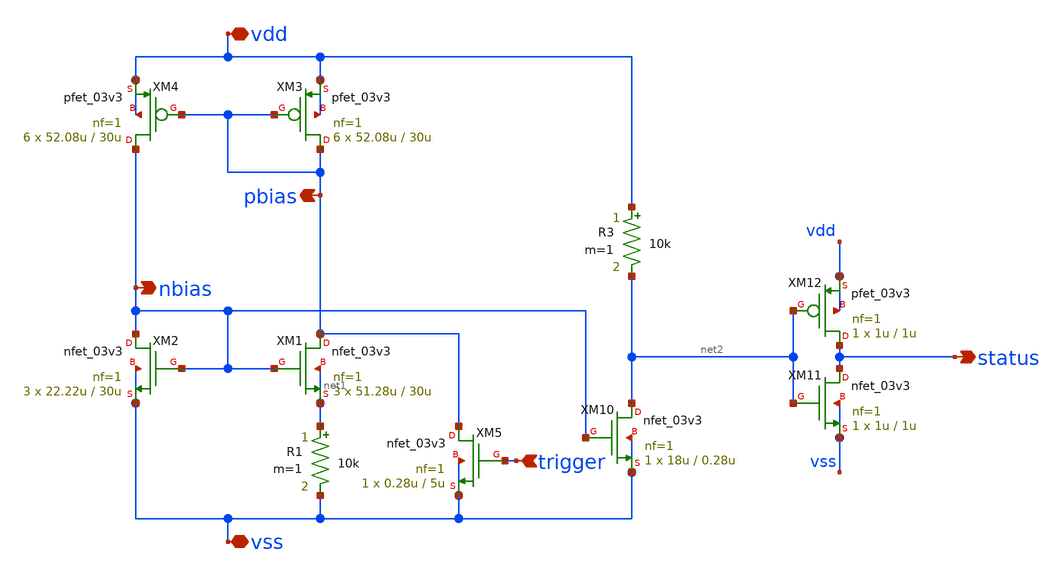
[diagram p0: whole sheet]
** sch_path: design/analog/beta multiplier/beta_multiplier.sch
**.subckt beta_multiplier vdd vss pbias nbias status trigger
*.iopin vdd
*.iopin vss
*.opin pbias
*.opin nbias
*.opin status
*.ipin trigger
XM1 pbias nbias net1 net1 nfet_03v3 L=30u W=51.28u nf=1 ad='int((nf+1)/2) * W/nf * 0.18u' as='int((nf+2)/2) * W/nf * 0.18u'
+ pd='2*int((nf+1)/2) * (W/nf + 0.18u)' ps='2*int((nf+2)/2) * (W/nf + 0.18u)' nrd='0.18u / W' nrs='0.18u / W'
+ sa=0 sb=0 sd=0 m=3
XM2 nbias nbias vss vss nfet_03v3 L=30u W=22.22u nf=1 ad='int((nf+1)/2) * W/nf * 0.18u' as='int((nf+2)/2) * W/nf * 0.18u'
+ pd='2*int((nf+1)/2) * (W/nf + 0.18u)' ps='2*int((nf+2)/2) * (W/nf + 0.18u)' nrd='0.18u / W' nrs='0.18u / W'
+ sa=0 sb=0 sd=0 m=3
XM3 pbias pbias vdd vdd pfet_03v3 L=30u W=52.08u nf=1 ad='int((nf+1)/2) * W/nf * 0.18u' as='int((nf+2)/2) * W/nf * 0.18u'
+ pd='2*int((nf+1)/2) * (W/nf + 0.18u)' ps='2*int((nf+2)/2) * (W/nf + 0.18u)' nrd='0.18u / W' nrs='0.18u / W'
+ sa=0 sb=0 sd=0 m=6
XM4 nbias pbias vdd vdd pfet_03v3 L=30u W=52.08u nf=1 ad='int((nf+1)/2) * W/nf * 0.18u' as='int((nf+2)/2) * W/nf * 0.18u'
+ pd='2*int((nf+1)/2) * (W/nf + 0.18u)' ps='2*int((nf+2)/2) * (W/nf + 0.18u)' nrd='0.18u / W' nrs='0.18u / W'
+ sa=0 sb=0 sd=0 m=6
R1 net1 vss 10k m=1
XM5 pbias trigger vss vss nfet_03v3 L=5u W=0.28u nf=1 ad='int((nf+1)/2) * W/nf * 0.18u' as='int((nf+2)/2) * W/nf * 0.18u'
+ pd='2*int((nf+1)/2) * (W/nf + 0.18u)' ps='2*int((nf+2)/2) * (W/nf + 0.18u)' nrd='0.18u / W' nrs='0.18u / W'
+ sa=0 sb=0 sd=0 m=1
XM10 net2 nbias vss vss nfet_03v3 L=0.28u W=18u nf=1 ad='int((nf+1)/2) * W/nf * 0.18u' as='int((nf+2)/2) * W/nf * 0.18u'
+ pd='2*int((nf+1)/2) * (W/nf + 0.18u)' ps='2*int((nf+2)/2) * (W/nf + 0.18u)' nrd='0.18u / W' nrs='0.18u / W'
+ sa=0 sb=0 sd=0 m=1
R3 vdd net2 10k m=1
XM11 status net2 vss vss nfet_03v3 L=1u W=1u nf=1 ad='int((nf+1)/2) * W/nf * 0.18u' as='int((nf+2)/2) * W/nf * 0.18u'
+ pd='2*int((nf+1)/2) * (W/nf + 0.18u)' ps='2*int((nf+2)/2) * (W/nf + 0.18u)' nrd='0.18u / W' nrs='0.18u / W'
+ sa=0 sb=0 sd=0 m=1
XM12 status net2 vdd vdd pfet_03v3 L=1u W=1u nf=1 ad='int((nf+1)/2) * W/nf * 0.18u' as='int((nf+2)/2) * W/nf * 0.18u'
+ pd='2*int((nf+1)/2) * (W/nf + 0.18u)' ps='2*int((nf+2)/2) * (W/nf + 0.18u)' nrd='0.18u / W' nrs='0.18u / W'
+ sa=0 sb=0 sd=0 m=1
**.ends
.end
